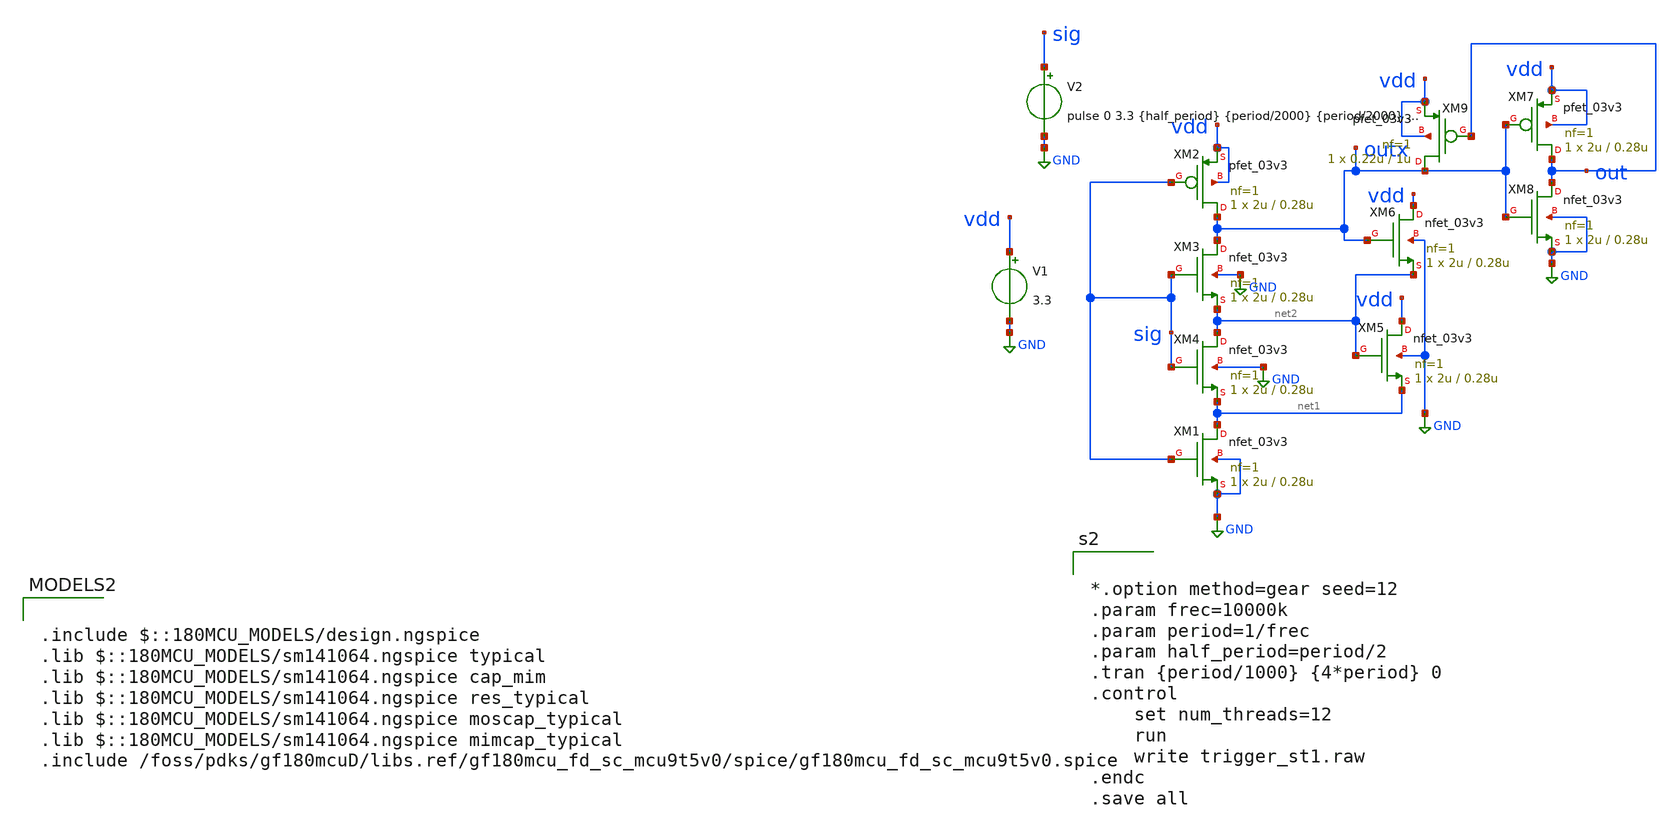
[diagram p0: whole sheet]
** sch_path: designs/libs/tb_trigger/trigger_st1.sch
**.subckt trigger_st1
XM2 outx sig vdd vdd pfet_03v3 L=0.28u W=2u nf=1 ad='int((nf+1)/2) * W/nf * 0.18u' as='int((nf+2)/2) * W/nf * 0.18u'
+ pd='2*int((nf+1)/2) * (W/nf + 0.18u)' ps='2*int((nf+2)/2) * (W/nf + 0.18u)' nrd='0.18u / W' nrs='0.18u / W'
+ sa=0 sb=0 sd=0 m=1
V2 sig GND pulse 0 3.3 {half_period} {period/2000} {period/2000} {half_period} {period}
V1 vdd GND 3.3
XM1 net1 sig GND GND nfet_03v3 L=0.28u W=2u nf=1 ad='int((nf+1)/2) * W/nf * 0.18u' as='int((nf+2)/2) * W/nf * 0.18u'
+ pd='2*int((nf+1)/2) * (W/nf + 0.18u)' ps='2*int((nf+2)/2) * (W/nf + 0.18u)' nrd='0.18u / W' nrs='0.18u / W'
+ sa=0 sb=0 sd=0 m=1
XM4 net2 sig net1 GND nfet_03v3 L=0.28u W=2u nf=1 ad='int((nf+1)/2) * W/nf * 0.18u' as='int((nf+2)/2) * W/nf * 0.18u'
+ pd='2*int((nf+1)/2) * (W/nf + 0.18u)' ps='2*int((nf+2)/2) * (W/nf + 0.18u)' nrd='0.18u / W' nrs='0.18u / W'
+ sa=0 sb=0 sd=0 m=1
XM3 outx sig net2 GND nfet_03v3 L=0.28u W=2u nf=1 ad='int((nf+1)/2) * W/nf * 0.18u' as='int((nf+2)/2) * W/nf * 0.18u'
+ pd='2*int((nf+1)/2) * (W/nf + 0.18u)' ps='2*int((nf+2)/2) * (W/nf + 0.18u)' nrd='0.18u / W' nrs='0.18u / W'
+ sa=0 sb=0 sd=0 m=1
XM5 vdd net2 net1 GND nfet_03v3 L=0.28u W=2u nf=1 ad='int((nf+1)/2) * W/nf * 0.18u' as='int((nf+2)/2) * W/nf * 0.18u'
+ pd='2*int((nf+1)/2) * (W/nf + 0.18u)' ps='2*int((nf+2)/2) * (W/nf + 0.18u)' nrd='0.18u / W' nrs='0.18u / W'
+ sa=0 sb=0 sd=0 m=1
XM6 vdd outx net2 GND nfet_03v3 L=0.28u W=2u nf=1 ad='int((nf+1)/2) * W/nf * 0.18u' as='int((nf+2)/2) * W/nf * 0.18u'
+ pd='2*int((nf+1)/2) * (W/nf + 0.18u)' ps='2*int((nf+2)/2) * (W/nf + 0.18u)' nrd='0.18u / W' nrs='0.18u / W'
+ sa=0 sb=0 sd=0 m=1
XM8 out outx GND GND nfet_03v3 L=0.28u W=2u nf=1 ad='int((nf+1)/2) * W/nf * 0.18u' as='int((nf+2)/2) * W/nf * 0.18u'
+ pd='2*int((nf+1)/2) * (W/nf + 0.18u)' ps='2*int((nf+2)/2) * (W/nf + 0.18u)' nrd='0.18u / W' nrs='0.18u / W'
+ sa=0 sb=0 sd=0 m=1
XM7 out outx vdd vdd pfet_03v3 L=0.28u W=2u nf=1 ad='int((nf+1)/2) * W/nf * 0.18u' as='int((nf+2)/2) * W/nf * 0.18u'
+ pd='2*int((nf+1)/2) * (W/nf + 0.18u)' ps='2*int((nf+2)/2) * (W/nf + 0.18u)' nrd='0.18u / W' nrs='0.18u / W'
+ sa=0 sb=0 sd=0 m=1
XM9 outx out vdd vdd pfet_03v3 L=1u W=0.22u nf=1 ad='int((nf+1)/2) * W/nf * 0.18u' as='int((nf+2)/2) * W/nf * 0.18u'
+ pd='2*int((nf+1)/2) * (W/nf + 0.18u)' ps='2*int((nf+2)/2) * (W/nf + 0.18u)' nrd='0.18u / W' nrs='0.18u / W'
+ sa=0 sb=0 sd=0 m=1
**** begin user architecture code

.include $::180MCU_MODELS/design.ngspice
.lib $::180MCU_MODELS/sm141064.ngspice typical
.lib $::180MCU_MODELS/sm141064.ngspice cap_mim
.lib $::180MCU_MODELS/sm141064.ngspice res_typical
.lib $::180MCU_MODELS/sm141064.ngspice moscap_typical
.lib $::180MCU_MODELS/sm141064.ngspice mimcap_typical
.include /foss/pdks/gf180mcuD/libs.ref/gf180mcu_fd_sc_mcu9t5v0/spice/gf180mcu_fd_sc_mcu9t5v0.spice



*.option method=gear seed=12
.param frec=10000k
.param period=1/frec
.param half_period=period/2
.tran {period/1000} {4*period} 0
.control
	set num_threads=12
	run
	write trigger_st1.raw
.endc
.save all


**** end user architecture code
**.ends
.GLOBAL GND
.end
